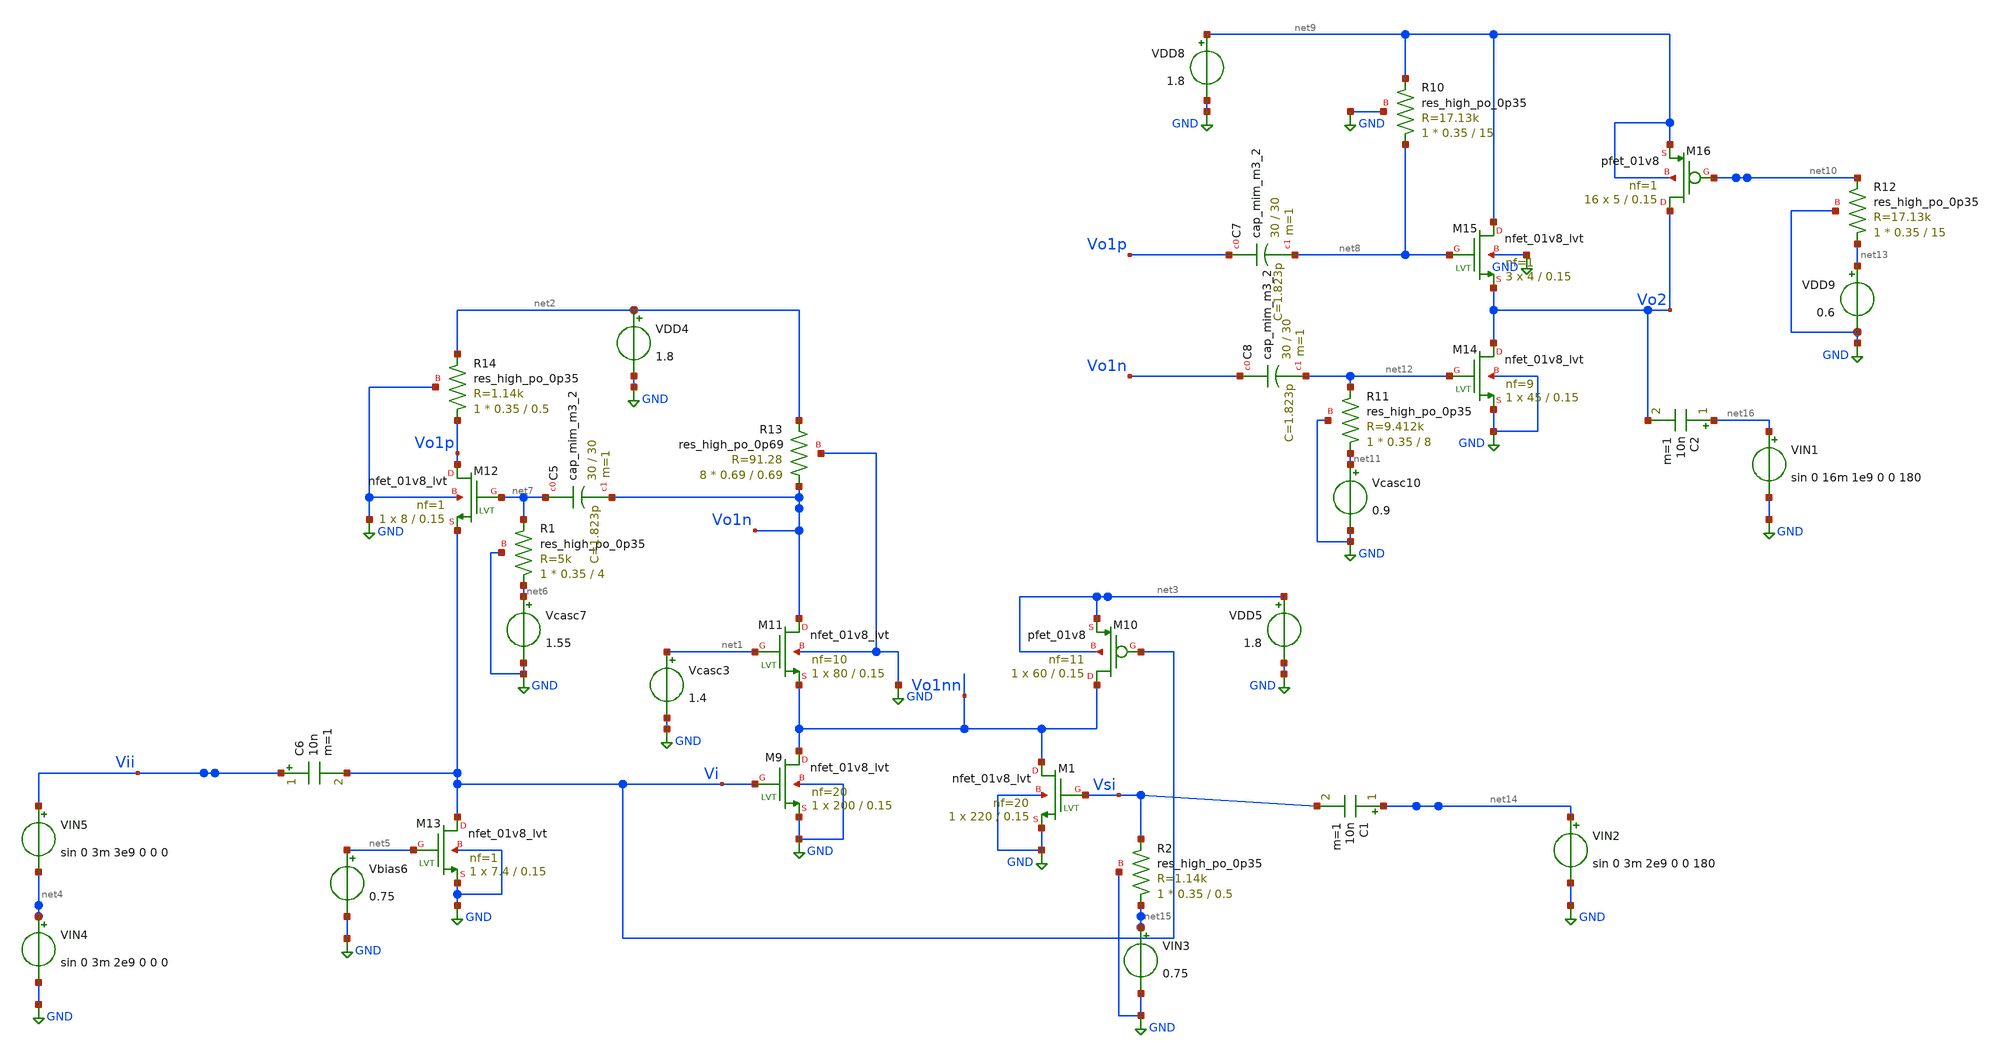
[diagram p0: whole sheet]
** sch_path: xschem/xschem4_sic_final/CompleteAMP6with50ohms.sch
**.subckt CompleteAMP6with50ohms
Vcasc3 net1 GND 1.4
VDD4 net2 GND 1.8
VDD5 net3 GND 1.8
Vbias6 net5 GND 0.75
Vcasc7 net6 GND 1.55
XR1 net6 net7 GND sky130_fd_pr__res_high_po_0p35 L=4 mult=1 m=1
XC5 net7 Vo1n sky130_fd_pr__cap_mim_m3_2 W=30 L=30 MF=1 m=1
C6 Vii Vi 10n m=1
XM9 Vo1nn Vi GND GND sky130_fd_pr__nfet_01v8_lvt L=0.15 W=200 nf=20 ad='int((nf+1)/2) * W/nf * 0.29'
+ as='int((nf+2)/2) * W/nf * 0.29' pd='2*int((nf+1)/2) * (W/nf + 0.29)' ps='2*int((nf+2)/2) * (W/nf + 0.29)'
+ nrd='0.29 / W' nrs='0.29 / W' sa=0 sb=0 sd=0 mult=1 m=1
XM10 Vo1nn Vi net3 net3 sky130_fd_pr__pfet_01v8 L=0.15 W=60 nf=11 ad='int((nf+1)/2) * W/nf * 0.29' as='int((nf+2)/2) * W/nf * 0.29'
+ pd='2*int((nf+1)/2) * (W/nf + 0.29)' ps='2*int((nf+2)/2) * (W/nf + 0.29)' nrd='0.29 / W' nrs='0.29 / W'
+ sa=0 sb=0 sd=0 mult=1 m=1
XM11 Vo1n net1 Vo1nn GND sky130_fd_pr__nfet_01v8_lvt L=0.15 W=80 nf=10 ad='int((nf+1)/2) * W/nf * 0.29'
+ as='int((nf+2)/2) * W/nf * 0.29' pd='2*int((nf+1)/2) * (W/nf + 0.29)' ps='2*int((nf+2)/2) * (W/nf + 0.29)'
+ nrd='0.29 / W' nrs='0.29 / W' sa=0 sb=0 sd=0 mult=1 m=1
XM12 Vo1p net7 Vi GND sky130_fd_pr__nfet_01v8_lvt L=0.15 W=8 nf=1 ad='int((nf+1)/2) * W/nf * 0.29' as='int((nf+2)/2) * W/nf * 0.29'
+ pd='2*int((nf+1)/2) * (W/nf + 0.29)' ps='2*int((nf+2)/2) * (W/nf + 0.29)' nrd='0.29 / W' nrs='0.29 / W'
+ sa=0 sb=0 sd=0 mult=1 m=1
XM13 Vi net5 GND GND sky130_fd_pr__nfet_01v8_lvt L=0.15 W=7.4 nf=1 ad='int((nf+1)/2) * W/nf * 0.29' as='int((nf+2)/2) * W/nf * 0.29'
+ pd='2*int((nf+1)/2) * (W/nf + 0.29)' ps='2*int((nf+2)/2) * (W/nf + 0.29)' nrd='0.29 / W' nrs='0.29 / W'
+ sa=0 sb=0 sd=0 mult=1 m=1
XM14 Vo2 net12 GND GND sky130_fd_pr__nfet_01v8_lvt L=0.15 W=45 nf=9 ad='int((nf+1)/2) * W/nf * 0.29'
+ as='int((nf+2)/2) * W/nf * 0.29' pd='2*int((nf+1)/2) * (W/nf + 0.29)' ps='2*int((nf+2)/2) * (W/nf + 0.29)'
+ nrd='0.29 / W' nrs='0.29 / W' sa=0 sb=0 sd=0 mult=1 m=1
XM15 net9 net8 Vo2 GND sky130_fd_pr__nfet_01v8_lvt L=0.15 W=4 nf=1 ad='int((nf+1)/2) * W/nf * 0.29' as='int((nf+2)/2) * W/nf * 0.29'
+ pd='2*int((nf+1)/2) * (W/nf + 0.29)' ps='2*int((nf+2)/2) * (W/nf + 0.29)' nrd='0.29 / W' nrs='0.29 / W'
+ sa=0 sb=0 sd=0 mult=3 m=3
XR10 net8 net9 GND sky130_fd_pr__res_high_po_0p35 L=15 mult=1 m=1
XM16 Vo2 net10 net9 net9 sky130_fd_pr__pfet_01v8 L=0.15 W=5 nf=1 ad='int((nf+1)/2) * W/nf * 0.29' as='int((nf+2)/2) * W/nf * 0.29'
+ pd='2*int((nf+1)/2) * (W/nf + 0.29)' ps='2*int((nf+2)/2) * (W/nf + 0.29)' nrd='0.29 / W' nrs='0.29 / W'
+ sa=0 sb=0 sd=0 mult=16 m=16
VDD8 net9 GND 1.8
VDD9 net13 GND 0.6
XC7 Vo1p net8 sky130_fd_pr__cap_mim_m3_2 W=30 L=30 MF=1 m=1
Vcasc10 net11 GND 0.9
XR11 net11 net12 GND sky130_fd_pr__res_high_po_0p35 L=8 mult=1 m=1
XC8 Vo1n net12 sky130_fd_pr__cap_mim_m3_2 W=30 L=30 MF=1 m=1
XR12 net13 net10 GND sky130_fd_pr__res_high_po_0p35 L=15 mult=1 m=1
XR14 Vo1p net2 GND sky130_fd_pr__res_high_po_0p35 L=0.5 mult=1 m=1
XM1 Vo1nn Vsi GND GND sky130_fd_pr__nfet_01v8_lvt L=0.15 W=220 nf=20 ad='int((nf+1)/2) * W/nf * 0.29'
+ as='int((nf+2)/2) * W/nf * 0.29' pd='2*int((nf+1)/2) * (W/nf + 0.29)' ps='2*int((nf+2)/2) * (W/nf + 0.29)'
+ nrd='0.29 / W' nrs='0.29 / W' sa=0 sb=0 sd=0 mult=1 m=1
VIN2 net14 GND sin 0 3m 2e9 0 0 180
C1 net14 Vsi 10n m=1
VIN3 net15 GND 0.75
VIN4 net4 GND sin 0 3m 2e9 0 0 0
XR13 Vo1n net2 GND sky130_fd_pr__res_high_po_0p69 L=0.69 mult=8 m=8
VIN1 net16 GND sin 0 16m 1e9 0 0 180
C2 net16 Vo2 10n m=1
VIN5 Vii net4 sin 0 3m 3e9 0 0 0
XR2 net15 Vsi GND sky130_fd_pr__res_high_po_0p35 L=0.5 mult=1 m=1
**** begin user architecture code

.lib $::SKYWATER_MODELS/sky130.lib.spice tt




.control
tran 1p 20n


print @m.xm9.msky130_fd_pr__nfet_01v8_lvt[id]
print @m.xm1.msky130_fd_pr__nfet_01v8_lvt[id]
print @m.xm10.msky130_fd_pr__pfet_01v8[id]
print @m.xm11.msky130_fd_pr__nfet_01v8_lvt[id]

print @m.xm9.msky130_fd_pr__nfet_01v8_lvt[vth]
print @m.xm1.msky130_fd_pr__nfet_01v8_lvt[vth]
print @m.xm10.msky130_fd_pr__pfet_01v8[vth]
print @m.xm11.msky130_fd_pr__nfet_01v8_lvt[vth]

print @m.xm9.msky130_fd_pr__nfet_01v8_lvt[gm]
print @m.xm1.msky130_fd_pr__nfet_01v8_lvt[gm]
print @m.xm10.msky130_fd_pr__pfet_01v8[gm]
print @m.xm11.msky130_fd_pr__nfet_01v8_lvt[gm]
print @m.xm12.msky130_fd_pr__nfet_01v8_lvt[gm]

plot v(Vo1nn)
#plot v(Vo1n)
plot v(VI)
plot v(Vsi)
#plot v(vo1nn)
spectrum 800MEG 5000MEG 100MEG v(Vo1nn)
let abc=spectrum 800MEG 5000MEG 100MEG v(Vo1nn)
plot db(abc)
#ac dec 100 1e9 10e9
#plot db(v(Vo1p)/v(VI))
.endc


**** end user architecture code
**.ends
.GLOBAL GND
.end
